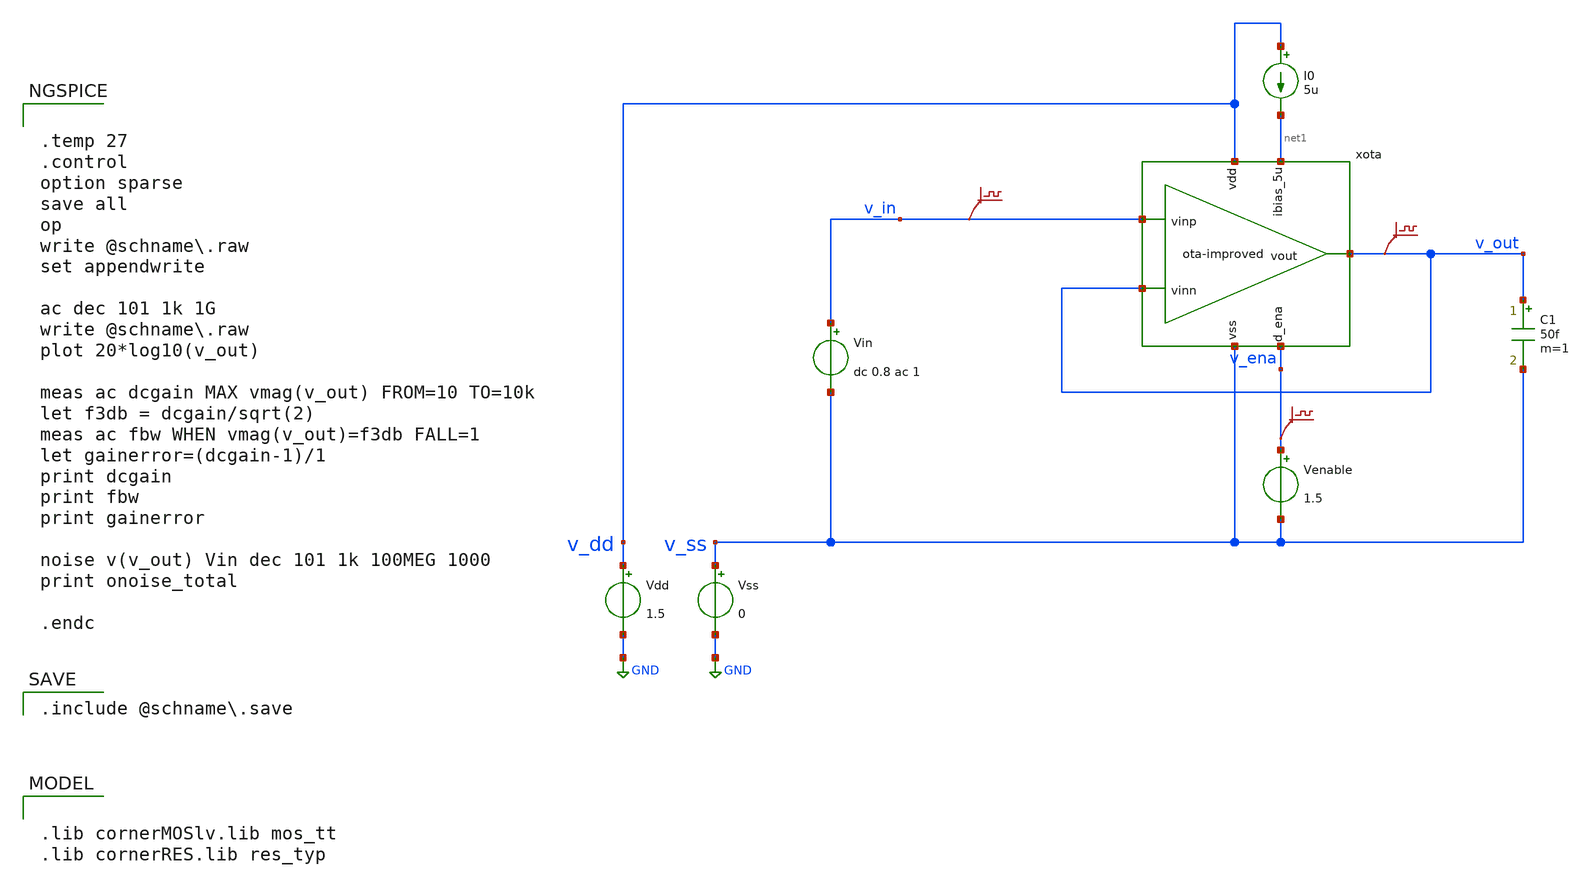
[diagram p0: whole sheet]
** sch_path: xschem/ota-improved_tb-ac.sch
* (c) 2024-2025 Harald Pretl, Apache-2.0 license
**.subckt ota-improved_tb-ac
Vdd v_dd GND 1.5
xota v_dd v_out v_in v_out net1 v_ena v_ss ota-improved
Vss v_ss GND 0
C1 v_out v_ss 50f m=1
Vin v_in v_ss dc 0.8 ac 1
I0 v_dd net1 5u
Venable v_ena v_ss 1.5
.save v(v_in)
.save v(v_out)
.save v(v_ena)
**** begin user architecture code

.lib cornerMOSlv.lib mos_tt
.lib cornerRES.lib res_typ



.temp 27
.control
option sparse
save all
op
write @schname\.raw
set appendwrite

ac dec 101 1k 1G
write @schname\.raw
plot 20*log10(v_out)

meas ac dcgain MAX vmag(v_out) FROM=10 TO=10k
let f3db = dcgain/sqrt(2)
meas ac fbw WHEN vmag(v_out)=f3db FALL=1
let gainerror=(dcgain-1)/1
print dcgain
print fbw
print gainerror

noise v(v_out) Vin dec 101 1k 100MEG 1000
print onoise_total

.endc


 .include @schname.save

**** end user architecture code
**.ends
.GLOBAL GND
.end
